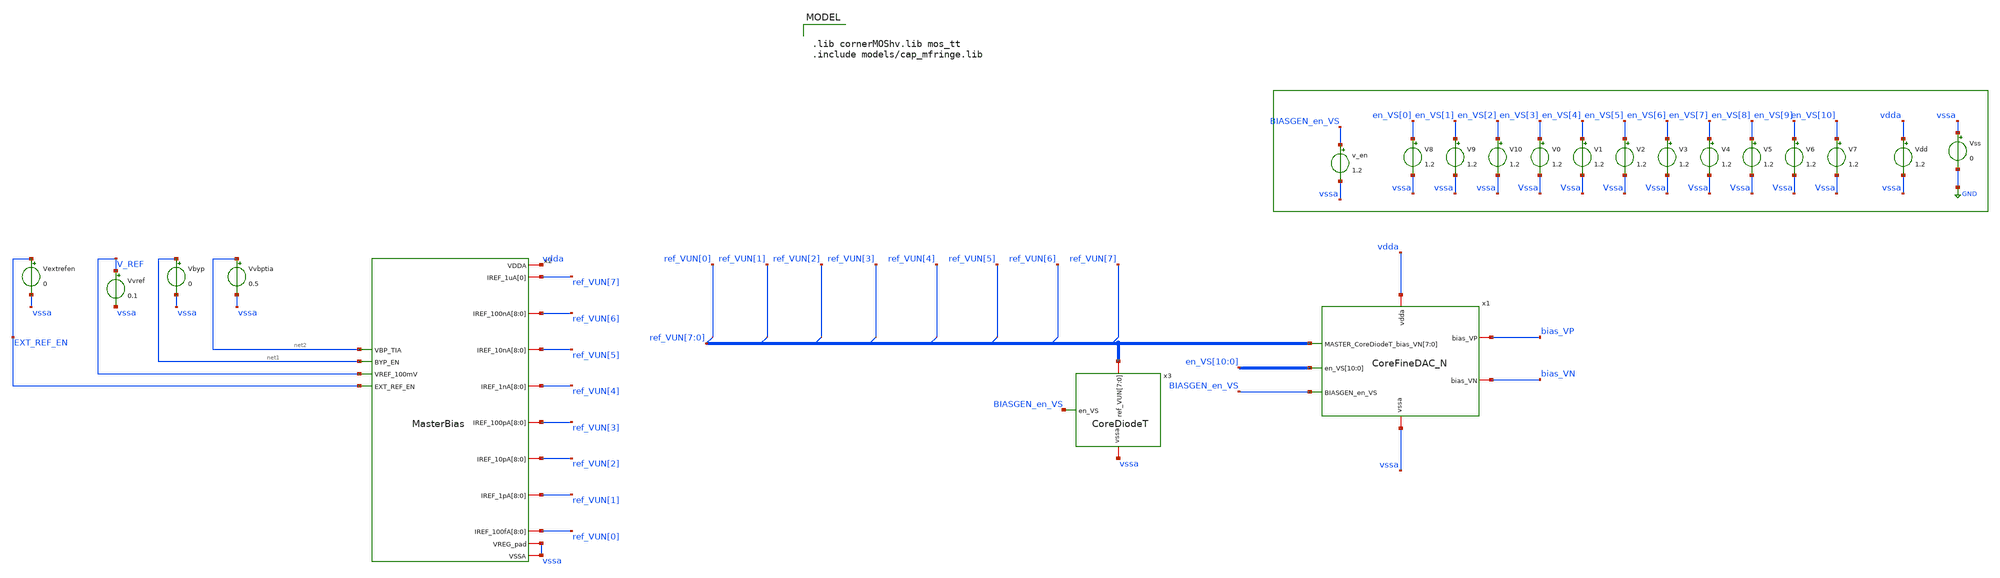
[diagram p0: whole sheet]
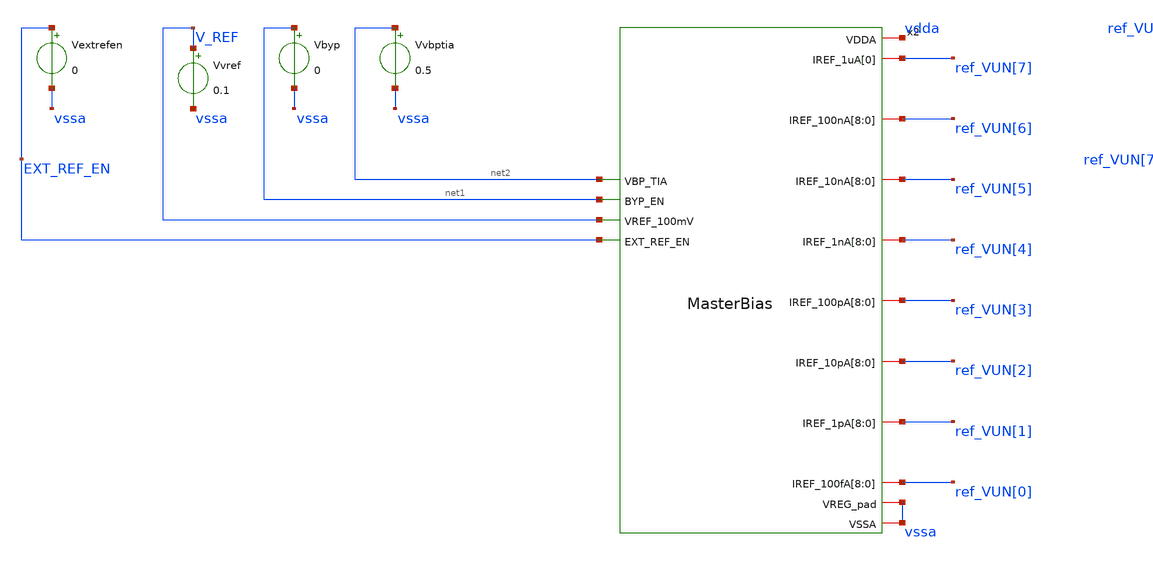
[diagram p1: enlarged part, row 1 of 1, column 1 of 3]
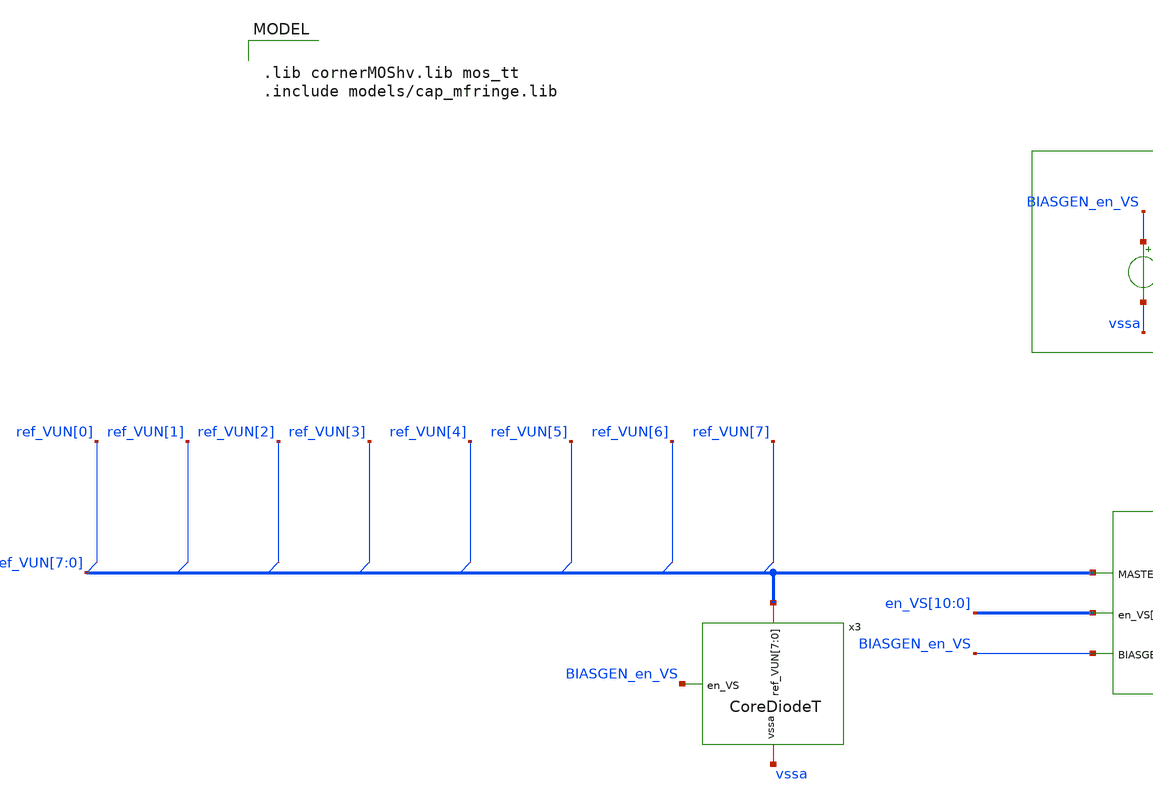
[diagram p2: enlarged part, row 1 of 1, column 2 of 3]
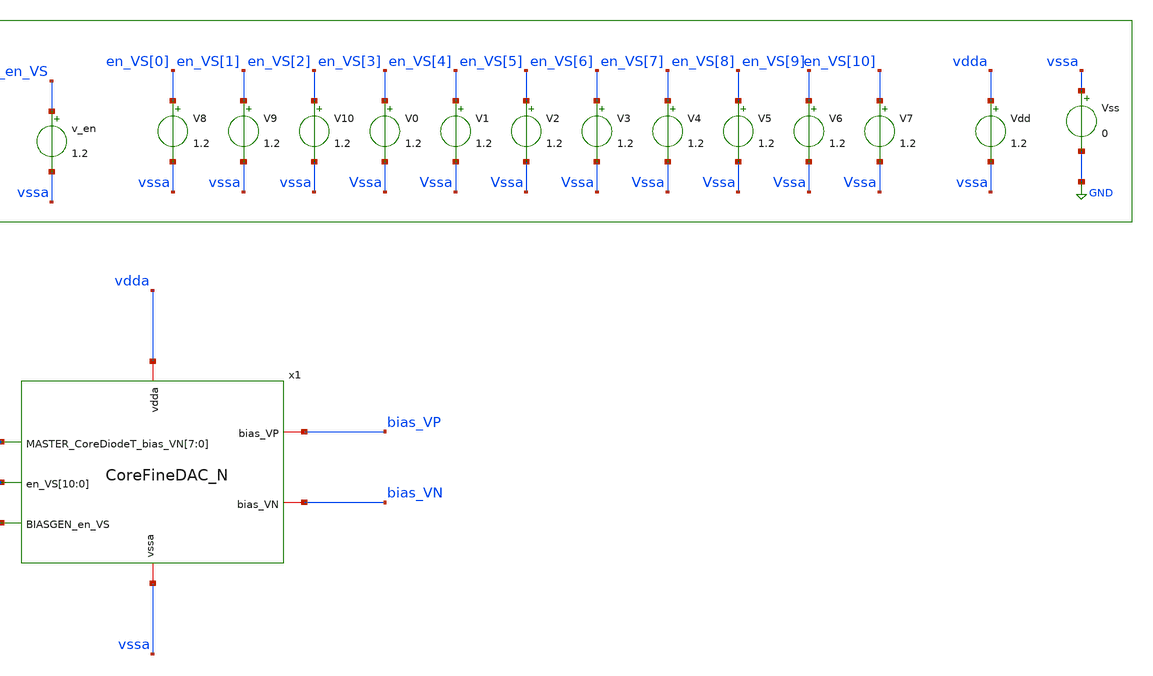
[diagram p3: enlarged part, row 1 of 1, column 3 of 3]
** sch_path: test_bench/CoreFineDAC_N_MasterBiais_dc_tb.sch
**.subckt CoreFineDAC_N_MasterBiais_dc_tb
Vdd vdda vssa 1.2
V0 en_VS[3] Vssa 1.2
Vss vssa GND 0
V1 en_VS[4] Vssa 1.2
V2 en_VS[5] Vssa 1.2
V3 en_VS[6] Vssa 1.2
V4 en_VS[7] Vssa 1.2
V5 en_VS[8] Vssa 1.2
V6 en_VS[9] Vssa 1.2
V7 en_VS[10] Vssa 1.2
V8 en_VS[0] vssa 1.2
V9 en_VS[1] vssa 1.2
V10 en_VS[2] vssa 1.2
v_en BIASGEN_en_VS vssa 1.2
x1 en_VS[10] en_VS[9] en_VS[8] en_VS[7] en_VS[6] en_VS[5] en_VS[4] en_VS[3] en_VS[2] en_VS[1]
+ en_VS[0] vssa vdda bias_VP bias_VN ref_VUN[7] ref_VUN[6] ref_VUN[5] ref_VUN[4] ref_VUN[3] ref_VUN[2]
+ ref_VUN[1] ref_VUN[0] BIASGEN_en_VS CoreFineDAC_N
x3 ref_VUN[7] ref_VUN[6] ref_VUN[5] ref_VUN[4] ref_VUN[3] ref_VUN[2] ref_VUN[1] ref_VUN[0] vssa
+ BIASGEN_en_VS CoreDiodeT
x2 net2 net1 V_REF EXT_REF_EN vdda ref_VUN[7] ref_VUN[6] ref_VUN[6] ref_VUN[6] ref_VUN[6] ref_VUN[6]
+ ref_VUN[6] ref_VUN[6] ref_VUN[6] ref_VUN[6] ref_VUN[5] ref_VUN[5] ref_VUN[5] ref_VUN[5] ref_VUN[5] ref_VUN[5]
+ ref_VUN[5] ref_VUN[5] ref_VUN[5] ref_VUN[4] ref_VUN[4] ref_VUN[4] ref_VUN[4] ref_VUN[4] ref_VUN[4] ref_VUN[4]
+ ref_VUN[4] ref_VUN[4] ref_VUN[3] ref_VUN[3] ref_VUN[3] ref_VUN[3] ref_VUN[3] ref_VUN[3] ref_VUN[3] ref_VUN[3]
+ ref_VUN[3] ref_VUN[2] ref_VUN[2] ref_VUN[2] ref_VUN[2] ref_VUN[2] ref_VUN[2] ref_VUN[2] ref_VUN[2] ref_VUN[2]
+ ref_VUN[1] ref_VUN[1] ref_VUN[1] ref_VUN[1] ref_VUN[1] ref_VUN[1] ref_VUN[1] ref_VUN[1] ref_VUN[1] ref_VUN[0]
+ ref_VUN[0] ref_VUN[0] ref_VUN[0] ref_VUN[0] ref_VUN[0] ref_VUN[0] ref_VUN[0] ref_VUN[0] vssa vssa MasterBias
Vbyp net1 vssa 0
Vextrefen EXT_REF_EN vssa 0
Vvbptia net2 vssa 0.5
Vvref V_REF vssa 0.1
**** begin user architecture code

.lib cornerMOShv.lib mos_tt
.include models/cap_mfringe.lib



.param temp=27
.options abstol=9e-16
.options gmin=9e-16
.options gmindc=9e-16
.control

nodeset v(x2.VBIAS)=0.5 v(x2.x_ota.vout1stage)=0.7 v(x2.x_ota.vpmirr)=0.35
let V_drain_ISINK_vect = vector(1)
let initial_range = 6
let code_range = initial_range
let max_range = initial_range +1
let digitalCommand = vector(1)
let out_UP = vector(1)
let V_out_UP = vector(1)
while code_range < max_range
    * Set the 3 bits
    alter V8 = 1.2*(code_range % 2)
    alter V9 = 1.2*(floor(code_range/2) % 2)
    alter V10 = 1.2*(floor(code_range/4) % 2)
    let min = 208
    let max = 224
    let code = max-1
    while code < max
      * save all
      * Set the 8 bits
      alter V0 = 1.2*(code % 2)
      alter V1 = 1.2*(floor(code/2) % 2)
      alter V2 = 1.2*(floor(code/4) % 2)
      alter V3 = 1.2*(floor(code/8) % 2)
      alter V4 = 1.2*(floor(code/16) % 2)
      alter V5 = 1.2*(floor(code/32) % 2)
      alter V6 = 1.2*(floor(code/64) % 2)
      alter V7 = 1.2*(floor(code/128) % 2)

      op

      let digitalCommand[0] = code
      let out_UP[0] = I(V.x1.V_out_UP)
      let V_out_UP[0] = I(V.x1.V_Ibias1)
      let V_drain_ISINK_vect[0] = V(x1.V_drain_ISINK)
      * let out_UP[code-min] = I(V.x1.V_Ibias1)
      let code = code + 1
      * print code
      * write CoreFineDAC_N_dc_tb/full_op_{$&code_range}.raw


   end
   setplot const
   settype current out_UP
   settype current V_out_UP
   settype voltage V_drain_ISINK_vect
   setscale digitalCommand
   plot out_UP
   plot V_out_UP
   plot V_drain_ISINK_vect

   let code_range = code_range + 1
   write  simulations/CoreFineDAC_N_MasterBiais_dc_tb/commandRange_{$&initial_range}_{$&max}.raw out_UP
+ V_out_UP V_drain_ISINK_vect
   * write CoreFineDAC_N_MasterBiais_dc_tb/commandRange_{$&initial_range}_{$&max}.raw out_UP
end


.endc





**** end user architecture code
**.ends
.GLOBAL GND
.end
